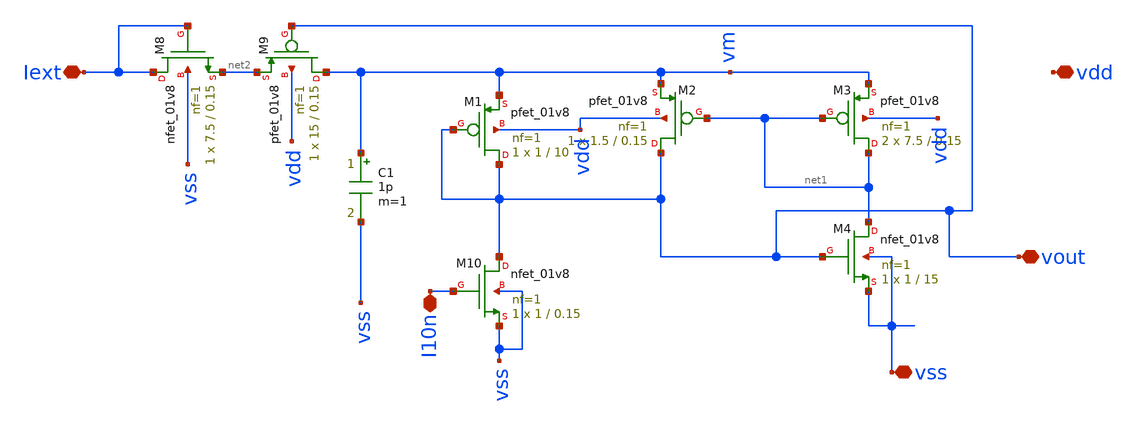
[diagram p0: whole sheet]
** sch_path: Neuron/ultralif/ultralif.sch
**.subckt ultralif Iext vout vss I10n vdd
*.iopin Iext
*.iopin vout
*.iopin vss
*.iopin I10n
*.iopin vdd
XM1 vout vout vm vdd sky130_fd_pr__pfet_01v8 L=10 W=1 nf=1 ad='int((nf+1)/2) * W/nf * 0.29' as='int((nf+2)/2) * W/nf * 0.29'
+ pd='2*int((nf+1)/2) * (W/nf + 0.29)' ps='2*int((nf+2)/2) * (W/nf + 0.29)' nrd='0.29 / W' nrs='0.29 / W'
+ sa=0 sb=0 sd=0 mult=1 m=1
XM2 vout net1 vm vdd sky130_fd_pr__pfet_01v8 L=0.15 W=1.5 nf=1 ad='int((nf+1)/2) * W/nf * 0.29' as='int((nf+2)/2) * W/nf * 0.29'
+ pd='2*int((nf+1)/2) * (W/nf + 0.29)' ps='2*int((nf+2)/2) * (W/nf + 0.29)' nrd='0.29 / W' nrs='0.29 / W'
+ sa=0 sb=0 sd=0 mult=1 m=1
XM3 net1 net1 vm vdd sky130_fd_pr__pfet_01v8 L=0.15 W=7.5 nf=1 ad='int((nf+1)/2) * W/nf * 0.29' as='int((nf+2)/2) * W/nf * 0.29'
+ pd='2*int((nf+1)/2) * (W/nf + 0.29)' ps='2*int((nf+2)/2) * (W/nf + 0.29)' nrd='0.29 / W' nrs='0.29 / W'
+ sa=0 sb=0 sd=0 mult=2 m=2
XM4 net1 vout vss vss sky130_fd_pr__nfet_01v8 L=15 W=1 nf=1 ad='int((1 + 1)/2) * 1 / 1 * 0.29' as='int((1 + 2)/2) * 1 / 1 * 0.29'
+ pd='2*int((1 + 1)/2) * (1 / 1 + 0.29)' ps='2*int((1 + 2)/2) * (1 / 1 + 0.29)' nrd='0.29 / 1 ' nrs='0.29 / 1 '
+ sa=0 sb=0 sd=0 mult=1 m=1
C1 vm vss 1p m=1
XM9 vm vout net2 vdd sky130_fd_pr__pfet_01v8 L=0.15 W=15 nf=1 ad='int((nf+1)/2) * W/nf * 0.29' as='int((nf+2)/2) * W/nf * 0.29'
+ pd='2*int((nf+1)/2) * (W/nf + 0.29)' ps='2*int((nf+2)/2) * (W/nf + 0.29)' nrd='0.29 / W' nrs='0.29 / W'
+ sa=0 sb=0 sd=0 mult=1 m=1
XM8 Iext Iext net2 vss sky130_fd_pr__nfet_01v8 L=0.15 W=7.5 nf=1 ad='int((1 + 1)/2) * 7.5 / 1 * 0.29'
+ as='int((1 + 2)/2) * 7.5 / 1 * 0.29' pd='2*int((1 + 1)/2) * (7.5 / 1 + 0.29)' ps='2*int((1 + 2)/2) * (7.5 / 1 + 0.29)'
+ nrd='0.29 / 7.5 ' nrs='0.29 / 7.5 ' sa=0 sb=0 sd=0 mult=1 m=1
XM10 vout I10n vss vss sky130_fd_pr__nfet_01v8 L=0.15 W=1 nf=1 ad='int((1 + 1)/2) * 1 / 1 * 0.29' as='int((1 + 2)/2) * 1 / 1 * 0.29'
+ pd='2*int((1 + 1)/2) * (1 / 1 + 0.29)' ps='2*int((1 + 2)/2) * (1 / 1 + 0.29)' nrd='0.29 / 1 ' nrs='0.29 / 1 '
+ sa=0 sb=0 sd=0 mult=1 m=1
**.ends
.end
